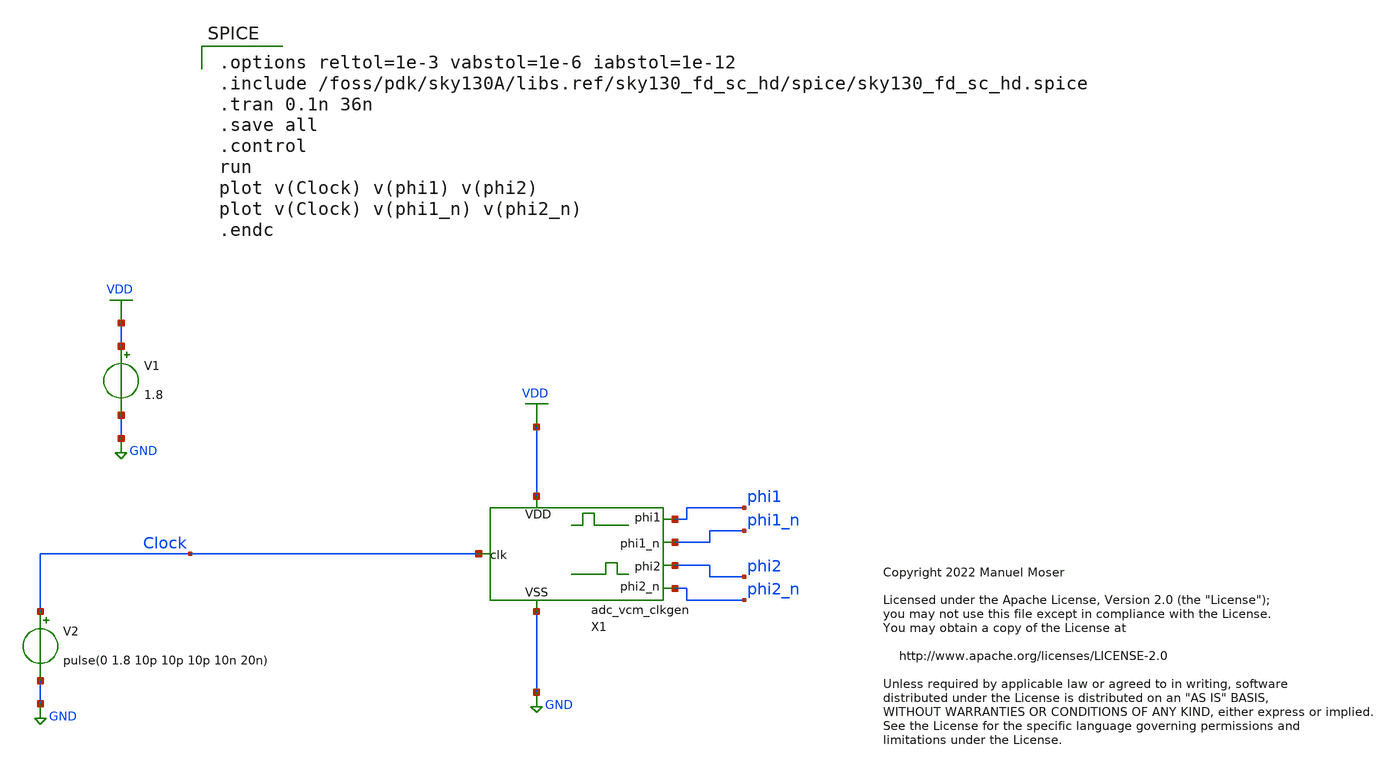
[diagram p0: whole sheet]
** sch_path: xschem/adc_vcm_clkgen_tb.sch
* Copyright 2022 Manuel Moser
* Licensed under the Apache License, Version 2.0 (the "License");
**.subckt adc_vcm_clkgen_tb
V1 VDD GND 1.8
V2 Clock GND pulse(0 1.8 10p 10p 10p 10n 20n)
X1 Clock VDD GND phi1_n phi1 phi2 phi2_n adc_vcm_clkgen
**** begin user architecture code

.options reltol=1e-3 vabstol=1e-6 iabstol=1e-12
.include /foss/pdk/sky130A/libs.ref/sky130_fd_sc_hd/spice/sky130_fd_sc_hd.spice
.tran 0.1n 36n
.save all
.control
run
plot v(Clock) v(phi1) v(phi2)
plot v(Clock) v(phi1_n) v(phi2_n)
.endc



** opencircuitdesign pdks install
.lib $::SKYWATER_MODELS/sky130.lib.spice tt


**** end user architecture code
**.ends

* expanding   symbol:  adc_vcm_clkgen.sym # of pins=7
** sym_path: xschem/adc_vcm_clkgen.sym
** sch_path: xschem/adc_vcm_clkgen.sch
.subckt adc_vcm_clkgen clk VDD VSS phi1_n phi1 phi2 phi2_n
*.iopin VDD
*.iopin VSS
*.opin phi2_n
*.opin phi2
*.opin phi1
*.opin phi1_n
*.ipin clk
x23 clk VSS VSS VDD VDD net5 sky130_fd_sc_hd__inv_1
x2 net6 VSS VSS VDD VDD phi1 sky130_fd_sc_hd__buf_4
x5 net6 VSS VSS VDD VDD net3 sky130_fd_sc_hd__inv_1
x11 net11 VSS VSS VDD VDD net6 sky130_fd_sc_hd__inv_1
x12 net7 VSS VSS VDD VDD net4 sky130_fd_sc_hd__inv_1
x4 net3 VSS VSS VDD VDD phi1_n sky130_fd_sc_hd__buf_4
x7 net4 VSS VSS VDD VDD phi2_n sky130_fd_sc_hd__buf_4
x8 net7 VSS VSS VDD VDD phi2 sky130_fd_sc_hd__buf_4
x3 net1 VSS VSS VDD VDD net8 sky130_fd_sc_hd__dlymetal6s6s_1
x10 net2 VSS VSS VDD VDD net9 sky130_fd_sc_hd__dlymetal6s6s_1
x6 net8 VSS VSS VDD VDD net10 sky130_fd_sc_hd__dlymetal6s6s_1
x13 net9 VSS VSS VDD VDD net13 sky130_fd_sc_hd__dlymetal6s6s_1
x1 net12 VSS VSS VDD VDD net7 sky130_fd_sc_hd__inv_1
x9 net10 VSS VSS VDD VDD net11 sky130_fd_sc_hd__dlymetal6s6s_1
x14 net13 VSS VSS VDD VDD net12 sky130_fd_sc_hd__dlymetal6s6s_1
x15 clk net4 VSS VSS VDD VDD net1 sky130_fd_sc_hd__nand2_1
x16 net3 net5 VSS VSS VDD VDD net2 sky130_fd_sc_hd__nand2_1
.ends

.GLOBAL GND
.GLOBAL VDD
.end
